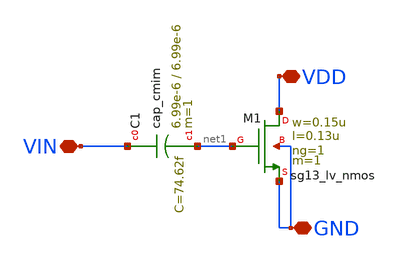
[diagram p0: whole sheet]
** sch_path: LVS/LAYOUT/test_capa/test_capa.sch
**.subckt test_capa VIN VDD GND
*.iopin VIN
*.iopin VDD
*.iopin GND
XC1 VIN net1 cap_cmim w=6.99e-6 l=6.99e-6 m=1 mm_ok=1
XM1 VDD net1 GND GND sg13_lv_nmos w=0.15u l=0.13u ng=1 m=1 mm_ok=1
**.ends
.end
